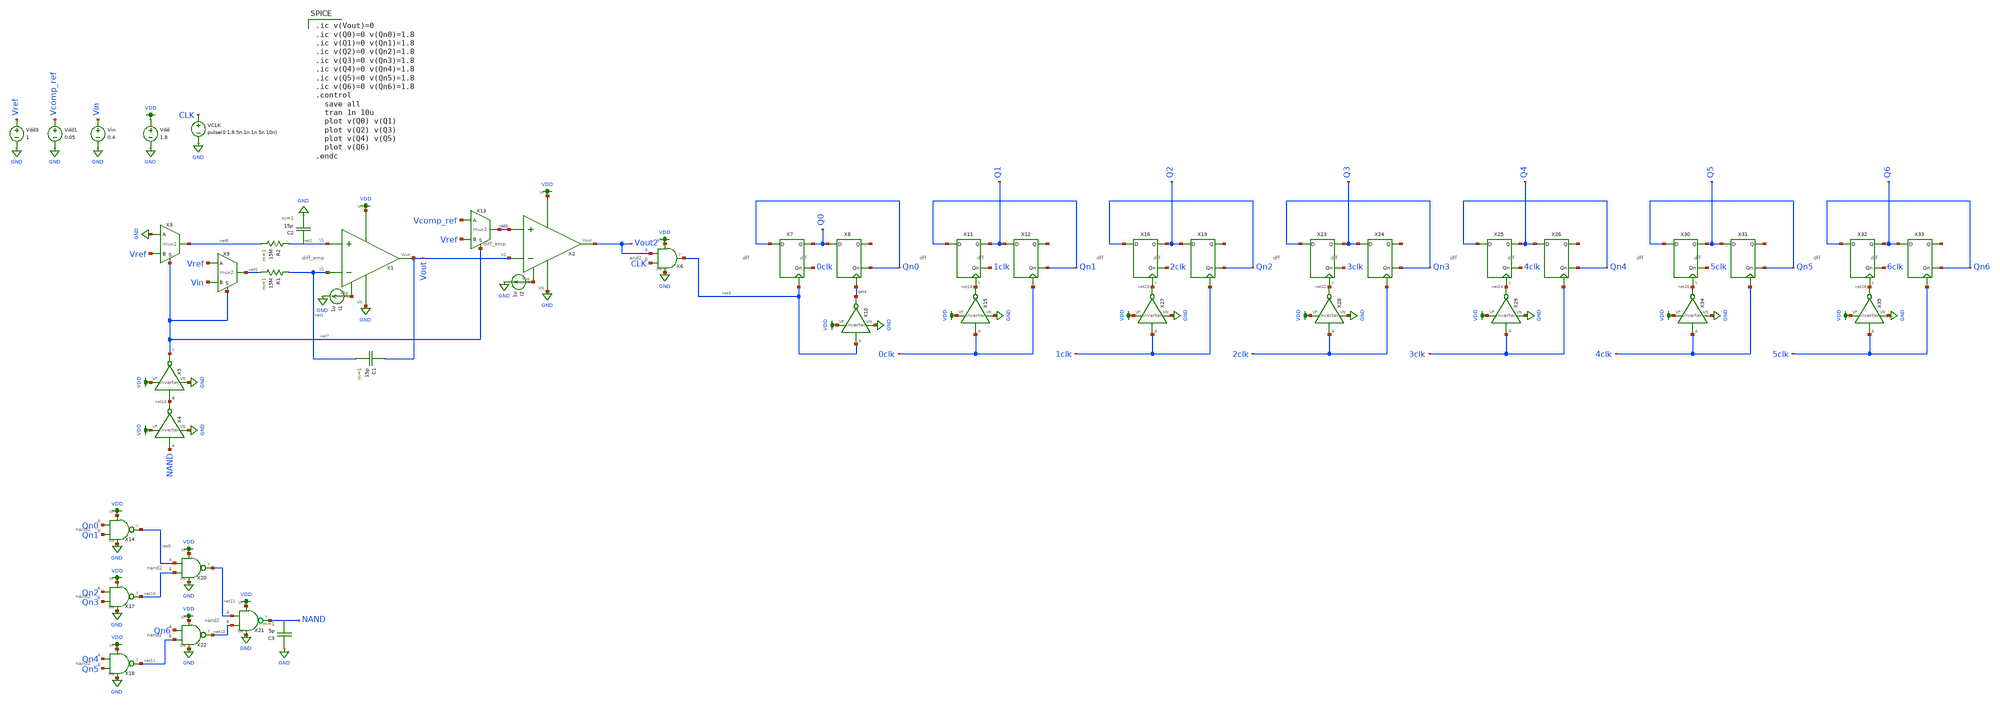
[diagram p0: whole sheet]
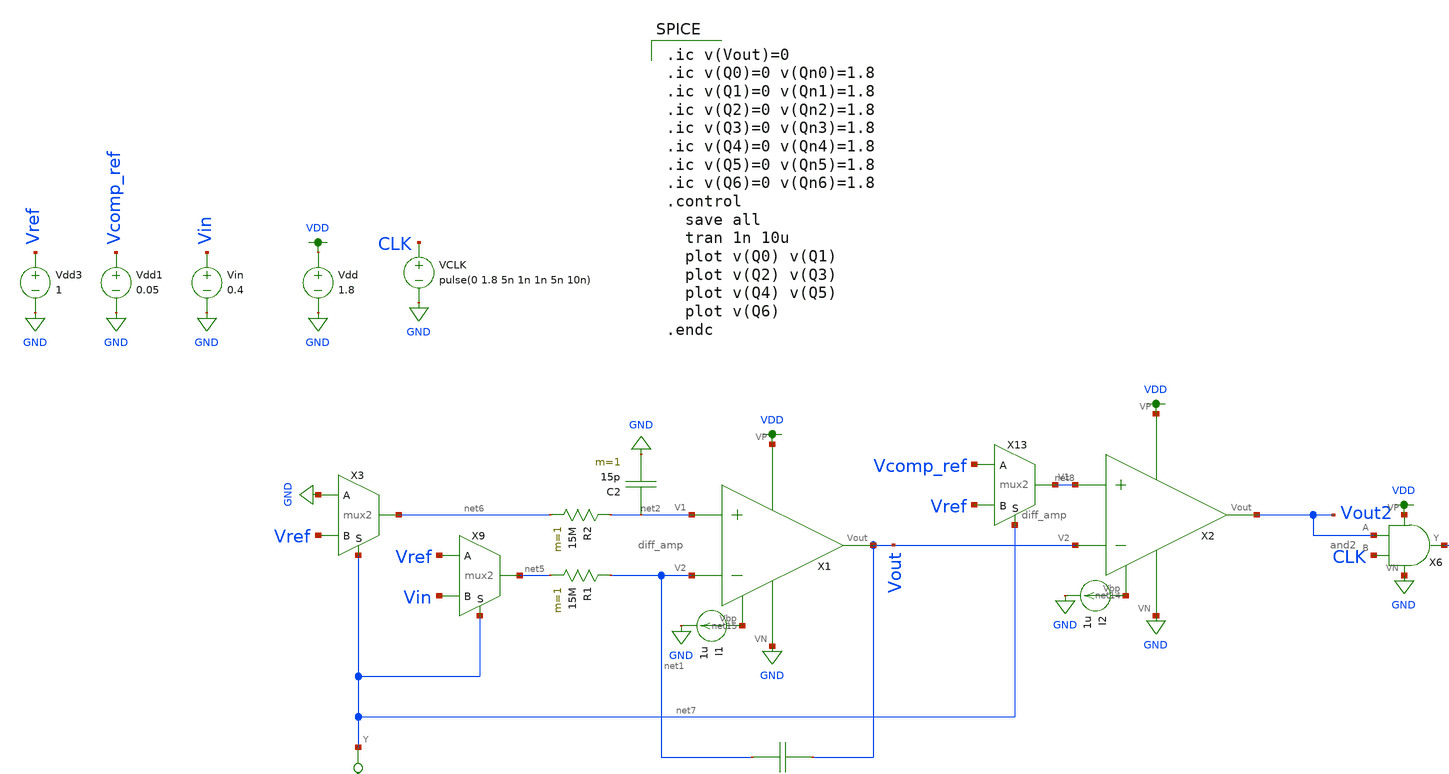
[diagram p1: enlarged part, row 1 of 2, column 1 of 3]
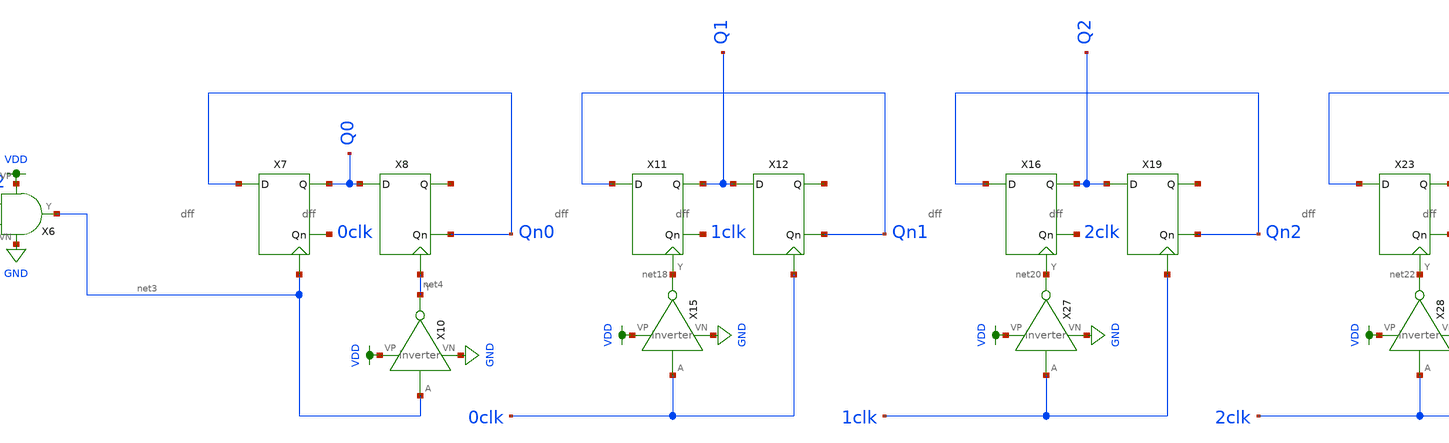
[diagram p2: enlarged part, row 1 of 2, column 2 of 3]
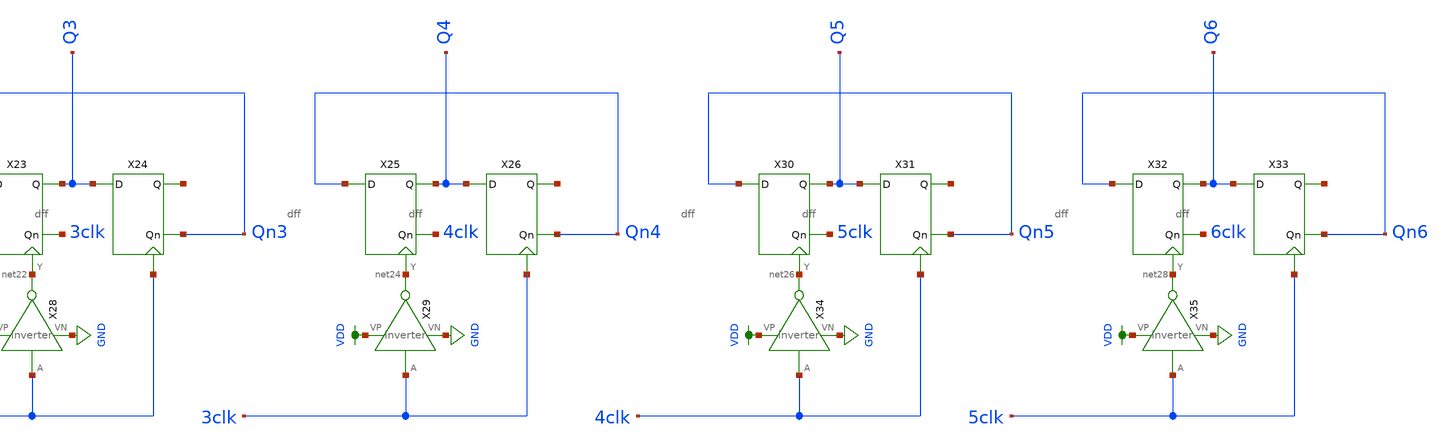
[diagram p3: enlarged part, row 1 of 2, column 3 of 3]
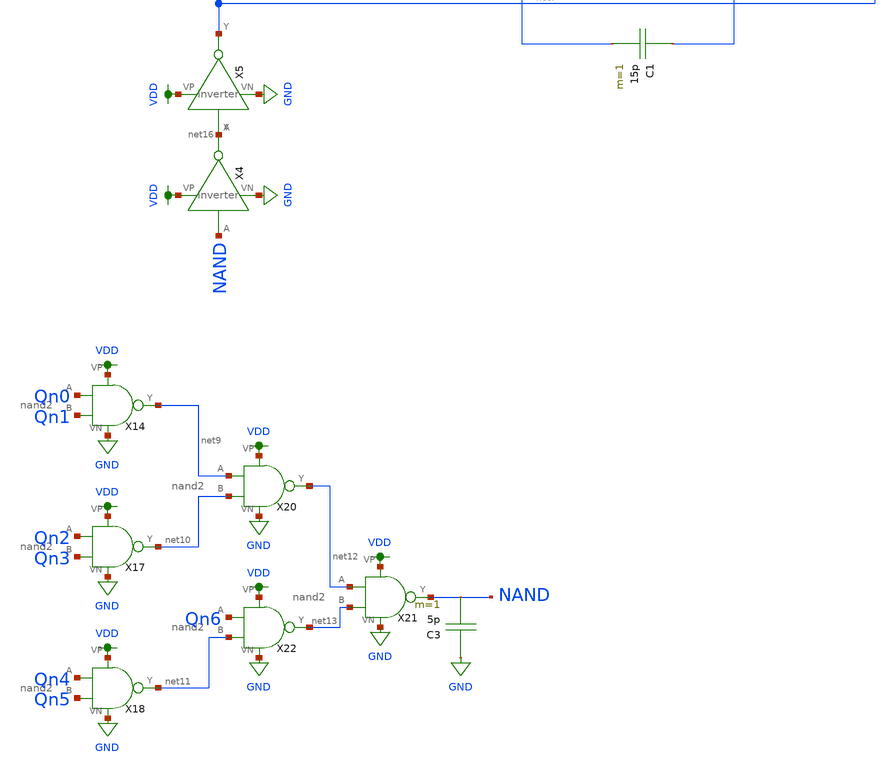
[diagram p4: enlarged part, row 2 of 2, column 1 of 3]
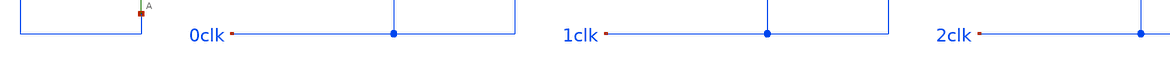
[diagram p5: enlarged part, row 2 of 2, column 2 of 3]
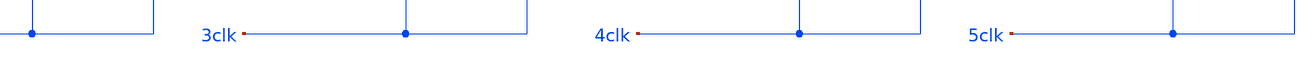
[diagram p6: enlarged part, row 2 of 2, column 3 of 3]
** sch_path: schematic/double-slope-thomas_new.sch
**.subckt double-slope-thomas_new
X2 VDD net14 Vout2 net8 Vout GND diff_amp
Vdd VDD GND 1.8
VCLK CLK GND pulse(0 1.8 5n 1n 1n 5n 10n)
Vdd1 Vcomp_ref GND 0.05
Vin Vin GND 0.4
I2 net14 GND 1u
C1 Vout net1 15p m=1
X1 VDD net15 Vout net2 net1 GND diff_amp
R1 net1 net5 15M m=1
C2 net2 GND 15p m=1
R2 net2 net6 15M m=1
I1 net15 GND 1u
Vdd3 Vref GND 1
X4 NAND net16 VDD GND inverter
X5 net16 net7 VDD GND inverter
X6 VDD Vout2 GND net3 CLK and2
X7 Qn0 0clk Q0 net3 dff
X8 Q0 Qn0 net17 net4 dff
X10 net3 net4 VDD GND inverter
X11 Qn1 1clk Q1 net18 dff
X12 Q1 Qn1 net19 0clk dff
X15 0clk net18 VDD GND inverter
X16 Qn2 2clk Q2 net20 dff
X19 Q2 Qn2 net21 1clk dff
X23 Qn3 3clk Q3 net22 dff
X24 Q3 Qn3 net23 2clk dff
X25 Qn4 4clk Q4 net24 dff
X26 Q4 Qn4 net25 3clk dff
X27 1clk net20 VDD GND inverter
X28 2clk net22 VDD GND inverter
X29 3clk net24 VDD GND inverter
X30 Qn5 5clk Q5 net26 dff
X31 Q5 Qn5 net27 4clk dff
X32 Qn6 6clk Q6 net28 dff
X33 Q6 Qn6 net29 5clk dff
X34 4clk net26 VDD GND inverter
X35 5clk net28 VDD GND inverter
X3 net6 GND Vref net7 mux2
X9 net5 Vref Vin net7 mux2
X13 net8 Vcomp_ref Vref net7 mux2
X14 Qn0 Qn1 net9 VDD GND nand2
X17 Qn2 Qn3 net10 VDD GND nand2
X18 Qn4 Qn5 net11 VDD GND nand2
X20 net9 net10 net12 VDD GND nand2
X21 net12 net13 NAND VDD GND nand2
X22 Qn6 net11 net13 VDD GND nand2
C3 GND NAND 5p m=1
**** begin user architecture code

.ic v(Vout)=0
.ic v(Q0)=0 v(Qn0)=1.8
.ic v(Q1)=0 v(Qn1)=1.8
.ic v(Q2)=0 v(Qn2)=1.8
.ic v(Q3)=0 v(Qn3)=1.8
.ic v(Q4)=0 v(Qn4)=1.8
.ic v(Q5)=0 v(Qn5)=1.8
.ic v(Q6)=0 v(Qn6)=1.8
.control
  save all
  tran 1n 10u
  plot v(Q0) v(Q1)
  plot v(Q2) v(Q3)
  plot v(Q4) v(Q5)
  plot v(Q6)
.endc


.option wnflag=1
.param MC_SWITCH=0.0
.lib ~/skywater/skywater-pdk/libraries/sky130_fd_pr_ngspice/latest/models/sky130.lib.spice tt

**** end user architecture code
**.ends
.GLOBAL GND
.GLOBAL VDD
.end
